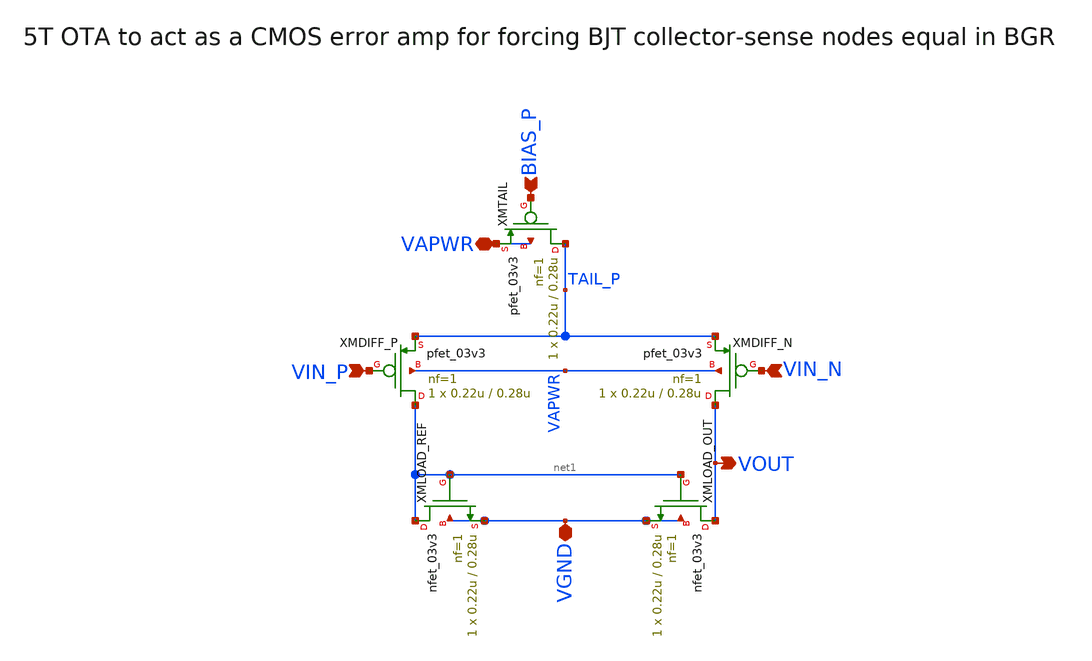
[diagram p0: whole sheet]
** sch_path: xschem/bgr_error_amp.sch
**.subckt bgr_error_amp VIN_P VIN_N BIAS_P VAPWR VGND VOUT
*.ipin VIN_P
*.ipin VIN_N
*.ipin BIAS_P
*.iopin VAPWR
*.iopin VGND
*.opin VOUT
XMDIFF_P net1 VIN_P TAIL_P VAPWR pfet_03v3 L=0.28u W=0.22u nf=1 ad='int((nf+1)/2) * W/nf * 0.18u' as='int((nf+2)/2) * W/nf * 0.18u'
+ pd='2*int((nf+1)/2) * (W/nf + 0.18u)' ps='2*int((nf+2)/2) * (W/nf + 0.18u)' nrd='0.18u / W' nrs='0.18u / W'
+ sa=0 sb=0 sd=0 m=1
XMDIFF_N VOUT VIN_N TAIL_P VAPWR pfet_03v3 L=0.28u W=0.22u nf=1 ad='int((nf+1)/2) * W/nf * 0.18u' as='int((nf+2)/2) * W/nf * 0.18u'
+ pd='2*int((nf+1)/2) * (W/nf + 0.18u)' ps='2*int((nf+2)/2) * (W/nf + 0.18u)' nrd='0.18u / W' nrs='0.18u / W'
+ sa=0 sb=0 sd=0 m=1
XMTAIL TAIL_P BIAS_P VAPWR VAPWR pfet_03v3 L=0.28u W=0.22u nf=1 ad='int((nf+1)/2) * W/nf * 0.18u' as='int((nf+2)/2) * W/nf * 0.18u'
+ pd='2*int((nf+1)/2) * (W/nf + 0.18u)' ps='2*int((nf+2)/2) * (W/nf + 0.18u)' nrd='0.18u / W' nrs='0.18u / W'
+ sa=0 sb=0 sd=0 m=1
XMLOAD_REF net1 net1 VGND VGND nfet_03v3 L=0.28u W=0.22u nf=1 ad='int((nf+1)/2) * W/nf * 0.18u' as='int((nf+2)/2) * W/nf * 0.18u'
+ pd='2*int((nf+1)/2) * (W/nf + 0.18u)' ps='2*int((nf+2)/2) * (W/nf + 0.18u)' nrd='0.18u / W' nrs='0.18u / W'
+ sa=0 sb=0 sd=0 m=1
XMLOAD_OUT VOUT net1 VGND VGND nfet_03v3 L=0.28u W=0.22u nf=1 ad='int((nf+1)/2) * W/nf * 0.18u' as='int((nf+2)/2) * W/nf * 0.18u'
+ pd='2*int((nf+1)/2) * (W/nf + 0.18u)' ps='2*int((nf+2)/2) * (W/nf + 0.18u)' nrd='0.18u / W' nrs='0.18u / W'
+ sa=0 sb=0 sd=0 m=1
**.ends
.end
